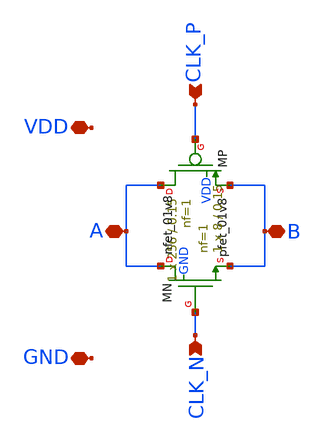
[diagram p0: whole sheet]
** sch_path: blocks/04_1Bit_DAC/xschem/TG_cell.sch
**.subckt TG_cell A B CLK_P CLK_N VDD GND
*.iopin A
*.iopin B
*.ipin CLK_P
*.ipin CLK_N
*.iopin VDD
*.iopin GND
XMP A CLK_P B VDD sky130_fd_pr__pfet_01v8 L=0.15 W=256 nf=1 ad='int((1 + 1)/2) * 256 / 1 * 0.29' as='int((1 + 2)/2) * 256 / 1 * 0.29'
+ pd='2*int((1 + 1)/2) * (256 / 1 + 0.29)' ps='2*int((1 + 2)/2) * (256 / 1 + 0.29)' nrd='0.29 / 256 ' nrs='0.29 / 256 '
+ sa=0 sb=0 sd=0 mult=1 m=1
XMN A CLK_N B GND sky130_fd_pr__nfet_01v8 L=0.15 W=8 nf=1 ad='int((1 + 1)/2) * 8 / 1 * 0.29' as='int((1 + 2)/2) * 8 / 1 * 0.29'
+ pd='2*int((1 + 1)/2) * (8 / 1 + 0.29)' ps='2*int((1 + 2)/2) * (8 / 1 + 0.29)' nrd='0.29 / 8 ' nrs='0.29 / 8 '
+ sa=0 sb=0 sd=0 mult=1 m=1
**.ends
.end
